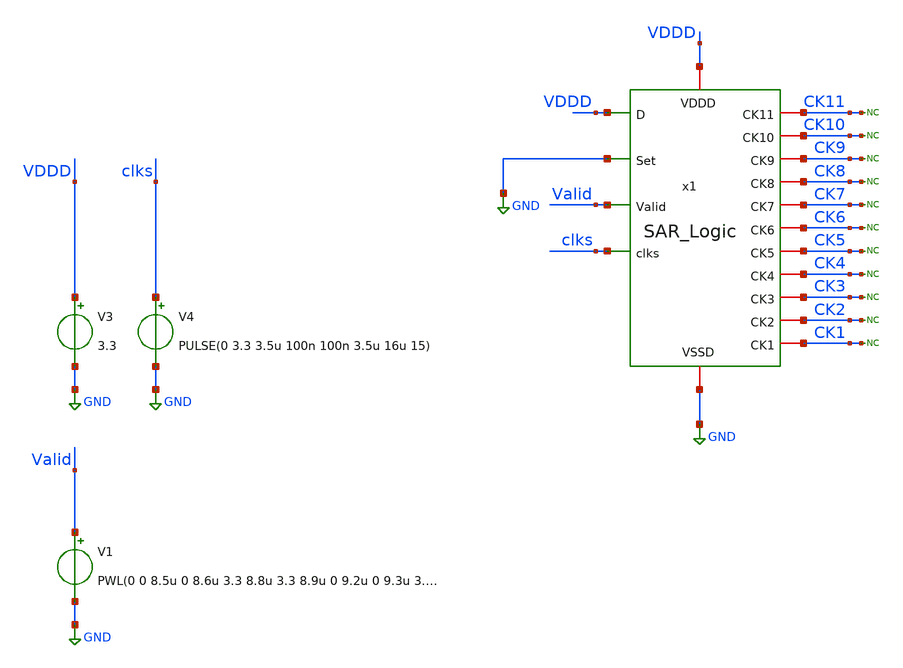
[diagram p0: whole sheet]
** sch_path: SAR_ADC/blocks/SAR_logic/SAR_Logic_tb.sch
**.subckt SAR_Logic_tb
x1 CK11 VDDD CK1 CK6 GND CK10 CK5 CK9 CK4 clks CK8 CK3 Valid CK2 CK7 GND VDDD SAR_Logic
* noconn CK11
* noconn CK10
* noconn CK9
* noconn CK8
* noconn CK7
* noconn CK6
* noconn CK5
* noconn CK4
* noconn CK3
* noconn CK2
* noconn CK1
V3 VDDD GND 3.3
V4 clks GND PULSE(0 3.3 3.5u 100n 100n 3.5u 16u 15)
V1 Valid GND PWL(0 0 8.5u 0 8.6u 3.3 8.8u 3.3 8.9u 0 9.2u 0 9.3u 3.3 9.5u 3.3 9.6u 0 9.9u 0 10u 3.3
+ 10.2u 3.3 10.3u 0 10.8u 0 10.9u 3.3 11.1u 3.3 11.2u 0 11.7u 0 11.8u 3.3 12u 3.3 12.1u 0 12.4u 0 12.5u 3.3
+ 12.7u 3.3 12.8u 0 13.1u 0 13.2u 3.3 13.4u 3.3 13.5u 0 13.8u 0 13.9u 3.3 14.1u 3.3 14.2u 0 14.5u 0 14.6u
+ 3.3 14.8u 3.3 14.9u 0 15.2u 0 15.3u 3.3 15.5u 3.3 15.6u 0 15.9 0 16u 3.3 16.2u 3.3 16.3u 0 16.6u 0
+ 16.7u 3.3 16.9u 3.3 17u 0 17.3u 0 17.4u 3.3 17.6u 3.3 17.8u 0 18u 0)
**** begin user architecture code



*Parameters
.options TEMPS= 27.0

*Models
.include /home/electrica/Documents/gf180_projects/pdk/gf180mcuC/libs.tech/ngspice/design.ngspice
.lib /home/electrica/Documents/gf180_projects/pdk/gf180mcuC/libs.tech/ngspice/sm141064.ngspice typical
.lib /home/electrica/Documents/gf180_projects/pdk/gf180mcuC/libs.tech/ngspice/smbb000149.ngspice typical


*Data to save
.save all

*Simulation
.control
tran 1n 30u
setplot dc1
plot V(Valid)+48 V(clks)+44 V(CK11)+40 V(CK10)+36 V(CK9)+32 V(CK8)+28 V(CK7)+24 V(CK6)+20 V(CK5)+16
+ V(CK4)+12 V(CK3)+8 V(CK2)+4 V(CK1)
set filetype=ascii
write SAR_Logic_tb_tran.raw

reset
unset filetype
op
save all
write SAR_Logic_tb.raw

.endc
.end



**** end user architecture code
**.ends
.GLOBAL GND
.end
